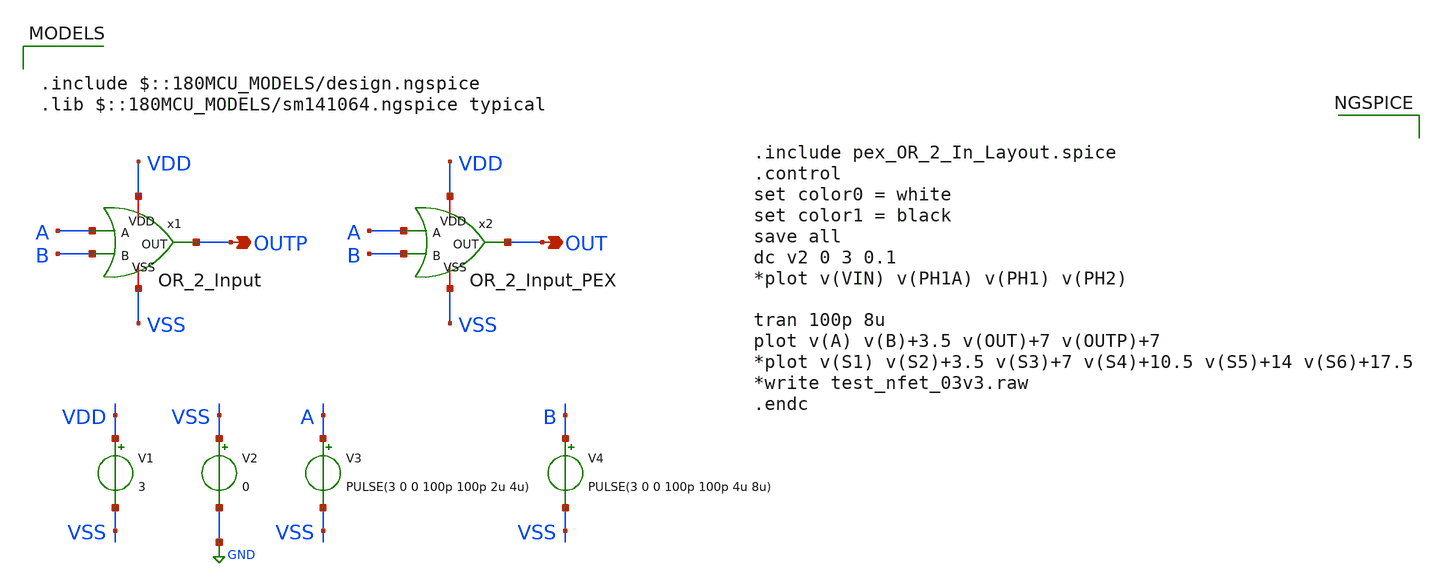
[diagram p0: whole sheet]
** sch_path: SCOP_INPUT_AND_MUX_PAKISTAN_03/Xschem/Logic_Gates/OR_2_Input_TB.sch
**.subckt OR_2_Input_TB OUTP OUT
*.opin OUTP
*.opin OUT
x1 VDD A B OUTP VSS OR_2_Input
V1 VDD VSS 3
V2 VSS GND 0
V3 A VSS PULSE(3 0 0 100p 100p 2u 4u)
V4 B VSS PULSE(3 0 0 100p 100p 4u 8u)
x2 VDD A B OUT VSS OR_2_Input_PEX
**** begin user architecture code

.include $::180MCU_MODELS/design.ngspice
.lib $::180MCU_MODELS/sm141064.ngspice typical



.include pex_OR_2_In_Layout.spice
.control
set color0 = white
set color1 = black
save all
dc v2 0 3 0.1
*plot v(VIN) v(PH1A) v(PH1) v(PH2)

tran 100p 8u
plot v(A) v(B)+3.5 v(OUT)+7 v(OUTP)+7
*plot v(S1) v(S2)+3.5 v(S3)+7 v(S4)+10.5 v(S5)+14 v(S6)+17.5
*write test_nfet_03v3.raw
.endc


**** end user architecture code
**.ends

* expanding   symbol:  OR_2_Input.sym # of pins=5
** sym_path: SCOP_INPUT_AND_MUX_PAKISTAN_03/Xschem/Logic_Gates/OR_2_Input.sym
** sch_path: SCOP_INPUT_AND_MUX_PAKISTAN_03/Xschem/Logic_Gates/OR_2_Input.sch
.subckt OR_2_Input VDD A B OUT VSS
*.ipin A
*.ipin B
*.iopin VDD
*.iopin VSS
*.opin OUT
XM1 net1 A VDD VDD pfet_03v3 L=0.28u W=2u nf=1 ad='int((nf+1)/2) * W/nf * 0.18u' as='int((nf+2)/2) * W/nf * 0.18u'
+ pd='2*int((nf+1)/2) * (W/nf + 0.18u)' ps='2*int((nf+2)/2) * (W/nf + 0.18u)' nrd='0.18u / W' nrs='0.18u / W'
+ sa=0 sb=0 sd=0 m=1
XM2 net2 B net1 VDD pfet_03v3 L=0.28u W=2u nf=1 ad='int((nf+1)/2) * W/nf * 0.18u' as='int((nf+2)/2) * W/nf * 0.18u'
+ pd='2*int((nf+1)/2) * (W/nf + 0.18u)' ps='2*int((nf+2)/2) * (W/nf + 0.18u)' nrd='0.18u / W' nrs='0.18u / W'
+ sa=0 sb=0 sd=0 m=1
XM3 net2 A VSS VSS nfet_03v3 L=0.28u W=0.5u nf=1 ad='int((nf+1)/2) * W/nf * 0.18u' as='int((nf+2)/2) * W/nf * 0.18u'
+ pd='2*int((nf+1)/2) * (W/nf + 0.18u)' ps='2*int((nf+2)/2) * (W/nf + 0.18u)' nrd='0.18u / W' nrs='0.18u / W'
+ sa=0 sb=0 sd=0 m=1
XM4 net2 B VSS VSS nfet_03v3 L=0.28u W=0.5u nf=1 ad='int((nf+1)/2) * W/nf * 0.18u' as='int((nf+2)/2) * W/nf * 0.18u'
+ pd='2*int((nf+1)/2) * (W/nf + 0.18u)' ps='2*int((nf+2)/2) * (W/nf + 0.18u)' nrd='0.18u / W' nrs='0.18u / W'
+ sa=0 sb=0 sd=0 m=1
XM8 OUT net2 VDD VDD pfet_03v3 L=0.28u W=1u nf=1 ad='int((nf+1)/2) * W/nf * 0.18u' as='int((nf+2)/2) * W/nf * 0.18u'
+ pd='2*int((nf+1)/2) * (W/nf + 0.18u)' ps='2*int((nf+2)/2) * (W/nf + 0.18u)' nrd='0.18u / W' nrs='0.18u / W'
+ sa=0 sb=0 sd=0 m=1
XM9 OUT net2 VSS VSS nfet_03v3 L=0.28u W=0.5u nf=1 ad='int((nf+1)/2) * W/nf * 0.18u' as='int((nf+2)/2) * W/nf * 0.18u'
+ pd='2*int((nf+1)/2) * (W/nf + 0.18u)' ps='2*int((nf+2)/2) * (W/nf + 0.18u)' nrd='0.18u / W' nrs='0.18u / W'
+ sa=0 sb=0 sd=0 m=1
.ends

.GLOBAL GND
.end
